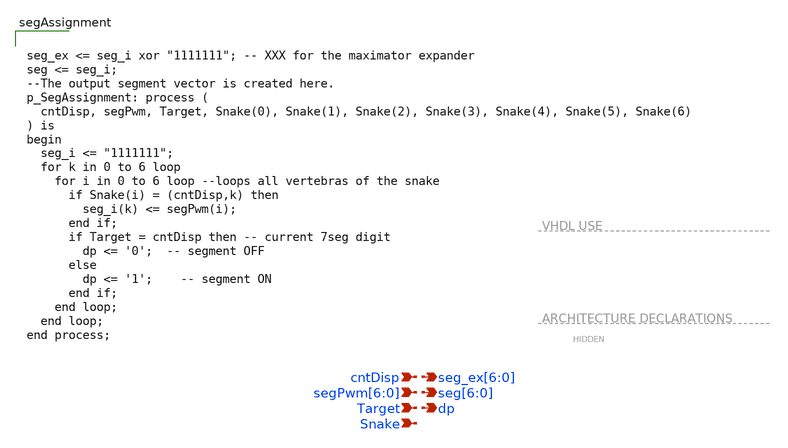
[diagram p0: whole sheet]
** sch_path: xschem/SegAssignment.sch
**.subckt SegAssignment Snake cntDisp seg[6],seg[5],seg[4],seg[3],seg[2],seg[1],seg[0]
*+ segPwm[6],segPwm[5],segPwm[4],segPwm[3],segPwm[2],segPwm[1],segPwm[0] Target dp seg_ex[6],seg_ex[5],seg_ex[4],seg_ex[3],seg_ex[2],seg_ex[1],seg_ex[0]
*.ipin Snake
*.ipin cntDisp
*.opin seg[6],seg[5],seg[4],seg[3],seg[2],seg[1],seg[0]
*.ipin segPwm[6],segPwm[5],segPwm[4],segPwm[3],segPwm[2],segPwm[1],segPwm[0]
*.ipin Target
*.opin dp
*.opin seg_ex[6],seg_ex[5],seg_ex[4],seg_ex[3],seg_ex[2],seg_ex[1],seg_ex[0]
**** begin user architecture code


seg_ex <= seg_i xor "1111111"; -- XXX for the maximator expander
seg <= seg_i;
--The output segment vector is created here.
p_SegAssignment: process (
  cntDisp, segPwm, Target, Snake(0), Snake(1), Snake(2), Snake(3), Snake(4), Snake(5), Snake(6)
) is
begin
  seg_i <= "1111111";
  for k in 0 to 6 loop
    for i in 0 to 6 loop --loops all vertebras of the snake
      if Snake(i) = (cntDisp,k) then
        seg_i(k) <= segPwm(i);
      end if;
      if Target = cntDisp then -- current 7seg digit
        dp <= '0';  -- segment OFF
      else
        dp <= '1';	-- segment ON
      end if;
    end loop;
  end loop;
end process;


**** end user architecture code
**.ends
.end
